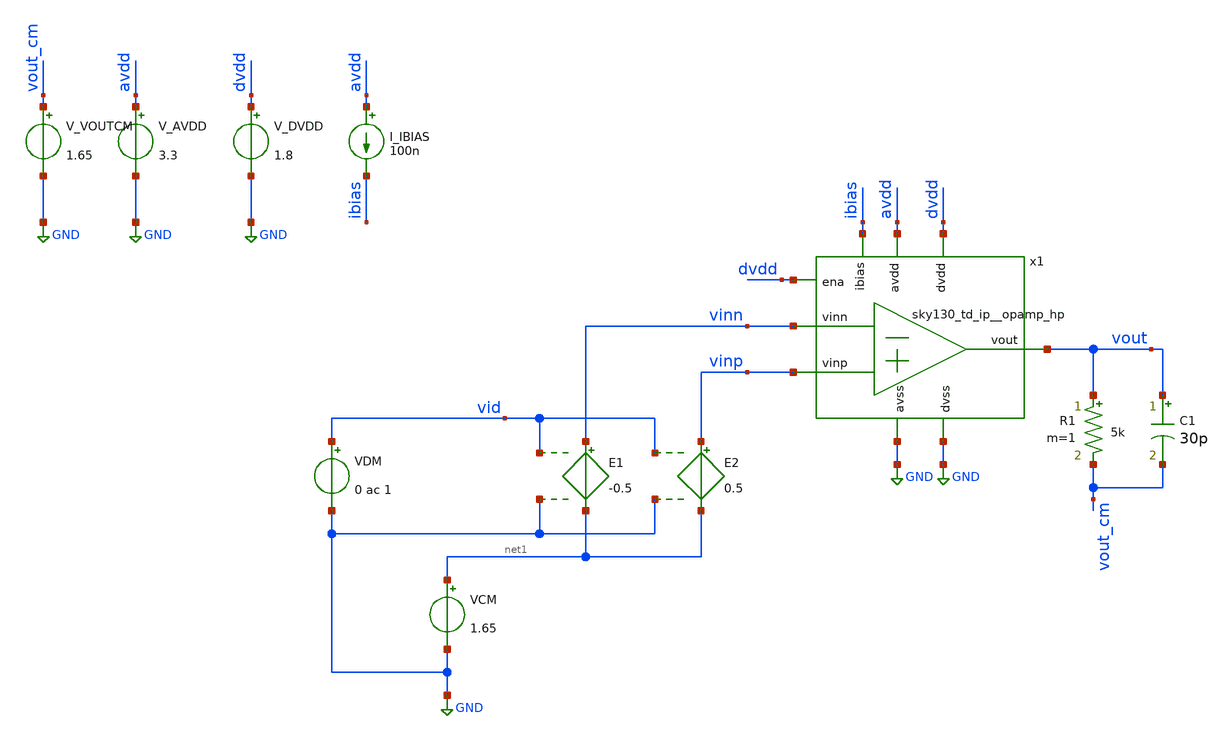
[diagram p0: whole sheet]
** sch_path: xschem/av0.sch
**.subckt av0
x1 avdd vout ibias vinn vinp GND dvdd GND dvdd sky130_td_ip__opamp_hp
V_AVDD avdd GND 3.3
.save i(v_avdd)
V_DVDD dvdd GND 1.8
.save i(v_dvdd)
I_IBIAS avdd ibias 100n
VCM net1 GND 1.65
R1 vout vout_cm 5k m=1
C1 vout vout_cm 30p m=1
V_VOUTCM vout_cm GND 1.65
.save i(v_voutcm)
E1 vinn net1 vid GND -0.5
VDM vid GND 0 ac 1
E2 vinp net1 vid GND 0.5
**** begin user architecture code


.save all

.control
save all


* Calculate input offset voltage
*dc VDM -100u 100u 5u
*run
*let vout = v(vout)
*meas DC input_offset_voltage WHEN vout=1.65
*let offset = $&input_offset_voltage
*alter VDM dc = $&input_offset_voltage
*alter VDM ac = 1
*echo offset = $&input_offset_voltage

* Run AC sweep from 1Hz to 1GHz
AC DEC 100 1 1000000000
run

* Get DC gain in DBs.
let av_db = db(vout / vid)
let av_lin = mag(vout / vid)
let ol_phase = 180/PI*phase(vout / vid)

meas AC av0_db FIND av_db AT=1
meas AC av0_lin FIND av_lin AT=1
let av0_minus_3 = av0_db - 3
meas AC fp1 WHEN av_db=av0_minus_3
meas AC ugf WHEN av_db=0
meas AC ol_phase_at_ugf FIND ol_phase AT=ugf

let pm = 180 + ol_phase_at_ugf
let gbw = av0_lin * fp1

echo
echo ===================================
echo Open-Loop characterization results:
echo - DC Gain: $&av0_db
echo - 3-dB frequency: $&fp1
echo - GBW: $&gbw
echo - PM: $&pm
echo ===================================


plot av_db ol_phase

.endc




.lib /usr/local/share/pdk/sky130A/libs.tech/combined/sky130.lib.spice tt
.option TEMP=27


**** end user architecture code
**.ends
.GLOBAL GND
.end
